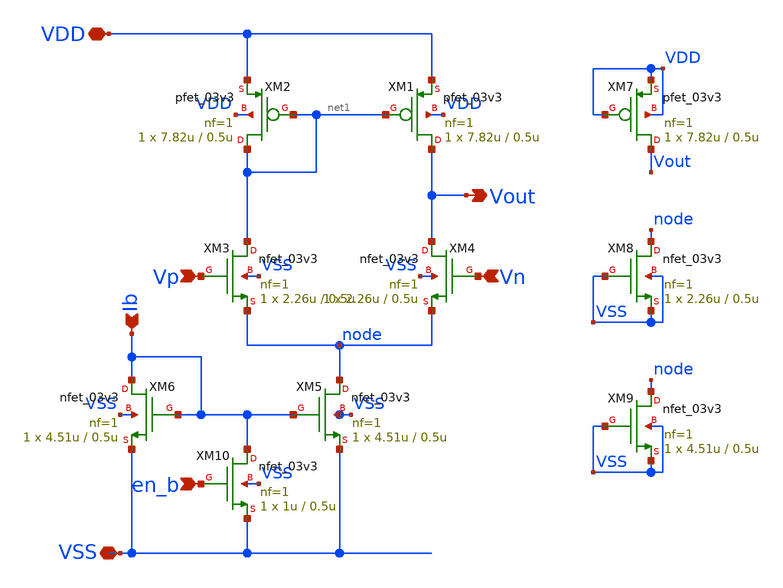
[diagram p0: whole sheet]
** sch_path: Analog/schematics/1_readout/ota5t_en.sch
**.subckt ota5t_en Vp Vn Vout VDD VSS Ib en_b
*.ipin Vp
*.ipin Vn
*.opin Vout
*.iopin VDD
*.iopin VSS
*.ipin Ib
*.ipin en_b
XM1 Vout net1 VDD VDD pfet_03v3 L=0.5u W=7.82u nf=1 ad='int((nf+1)/2) * W/nf * 0.18u' as='int((nf+2)/2) * W/nf * 0.18u'
+ pd='2*int((nf+1)/2) * (W/nf + 0.18u)' ps='2*int((nf+2)/2) * (W/nf + 0.18u)' nrd='0.18u / W' nrs='0.18u / W'
+ sa=0 sb=0 sd=0 m=1
XM2 net1 net1 VDD VDD pfet_03v3 L=0.5u W=7.82u nf=1 ad='int((nf+1)/2) * W/nf * 0.18u' as='int((nf+2)/2) * W/nf * 0.18u'
+ pd='2*int((nf+1)/2) * (W/nf + 0.18u)' ps='2*int((nf+2)/2) * (W/nf + 0.18u)' nrd='0.18u / W' nrs='0.18u / W'
+ sa=0 sb=0 sd=0 m=1
XM3 net1 Vp node VSS nfet_03v3 L=0.5u W=2.26u nf=1 ad='int((nf+1)/2) * W/nf * 0.18u' as='int((nf+2)/2) * W/nf * 0.18u'
+ pd='2*int((nf+1)/2) * (W/nf + 0.18u)' ps='2*int((nf+2)/2) * (W/nf + 0.18u)' nrd='0.18u / W' nrs='0.18u / W'
+ sa=0 sb=0 sd=0 m=1
XM4 Vout Vn node VSS nfet_03v3 L=0.5u W=2.26u nf=1 ad='int((nf+1)/2) * W/nf * 0.18u' as='int((nf+2)/2) * W/nf * 0.18u'
+ pd='2*int((nf+1)/2) * (W/nf + 0.18u)' ps='2*int((nf+2)/2) * (W/nf + 0.18u)' nrd='0.18u / W' nrs='0.18u / W'
+ sa=0 sb=0 sd=0 m=1
XM5 node Ib VSS VSS nfet_03v3 L=0.5u W=4.51u nf=1 ad='int((nf+1)/2) * W/nf * 0.18u' as='int((nf+2)/2) * W/nf * 0.18u'
+ pd='2*int((nf+1)/2) * (W/nf + 0.18u)' ps='2*int((nf+2)/2) * (W/nf + 0.18u)' nrd='0.18u / W' nrs='0.18u / W'
+ sa=0 sb=0 sd=0 m=1
XM6 Ib Ib VSS VSS nfet_03v3 L=0.5u W=4.51u nf=1 ad='int((nf+1)/2) * W/nf * 0.18u' as='int((nf+2)/2) * W/nf * 0.18u'
+ pd='2*int((nf+1)/2) * (W/nf + 0.18u)' ps='2*int((nf+2)/2) * (W/nf + 0.18u)' nrd='0.18u / W' nrs='0.18u / W'
+ sa=0 sb=0 sd=0 m=1
XM7 Vout VDD VDD VDD pfet_03v3 L=0.5u W=7.82u nf=1 ad='int((nf+1)/2) * W/nf * 0.18u' as='int((nf+2)/2) * W/nf * 0.18u'
+ pd='2*int((nf+1)/2) * (W/nf + 0.18u)' ps='2*int((nf+2)/2) * (W/nf + 0.18u)' nrd='0.18u / W' nrs='0.18u / W'
+ sa=0 sb=0 sd=0 m=1
XM8 node VSS VSS VSS nfet_03v3 L=0.5u W=2.26u nf=1 ad='int((nf+1)/2) * W/nf * 0.18u' as='int((nf+2)/2) * W/nf * 0.18u'
+ pd='2*int((nf+1)/2) * (W/nf + 0.18u)' ps='2*int((nf+2)/2) * (W/nf + 0.18u)' nrd='0.18u / W' nrs='0.18u / W'
+ sa=0 sb=0 sd=0 m=1
XM9 node VSS VSS VSS nfet_03v3 L=0.5u W=4.51u nf=1 ad='int((nf+1)/2) * W/nf * 0.18u' as='int((nf+2)/2) * W/nf * 0.18u'
+ pd='2*int((nf+1)/2) * (W/nf + 0.18u)' ps='2*int((nf+2)/2) * (W/nf + 0.18u)' nrd='0.18u / W' nrs='0.18u / W'
+ sa=0 sb=0 sd=0 m=1
XM10 Ib en_b VSS VSS nfet_03v3 L=0.5u W=1u nf=1 ad='int((nf+1)/2) * W/nf * 0.18u' as='int((nf+2)/2) * W/nf * 0.18u'
+ pd='2*int((nf+1)/2) * (W/nf + 0.18u)' ps='2*int((nf+2)/2) * (W/nf + 0.18u)' nrd='0.18u / W' nrs='0.18u / W'
+ sa=0 sb=0 sd=0 m=1
**.ends
.end
